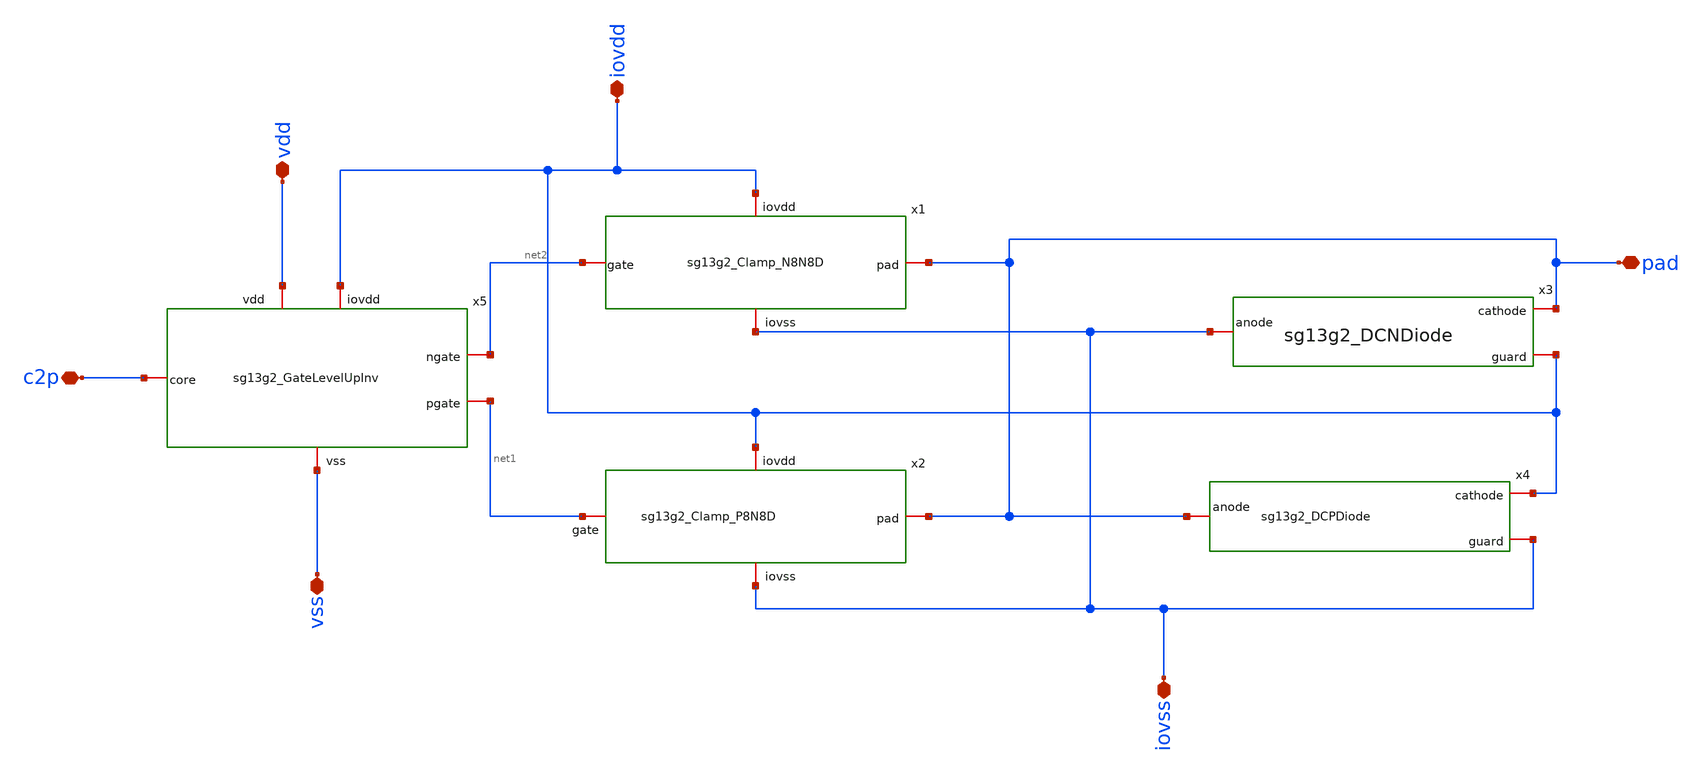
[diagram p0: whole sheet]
** sch_path: CDR4176-main/schematic/xschem/project_io/sg13g2_IOPadOut16mA/sg13g2_IOPadOut16mA.sch
**.subckt sg13g2_IOPadOut16mA iovss pad vss c2p vdd iovdd
*.iopin iovss
*.iopin pad
*.iopin vss
*.iopin c2p
*.iopin vdd
*.iopin iovdd
x1 iovdd pad net2 iovss sg13g2_Clamp_N8N8D
x3 pad iovss iovdd sg13g2_DCNDiode
x4 iovdd pad iovss sg13g2_DCPDiode
x5 vdd iovdd net2 net1 c2p vss sg13g2_GateLevelUpInv
x2 iovdd net1 pad iovss sg13g2_Clamp_P8N8D
**.ends
.end
